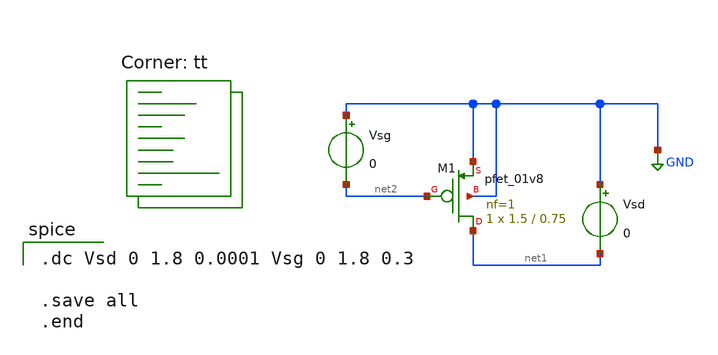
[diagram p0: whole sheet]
** sch_path: pmos_test.sch
**.subckt pmos_test
XM1 net1 net2 GND GND sky130_fd_pr__pfet_01v8 L=0.75 W=1.5 nf=1 ad='int((nf+1)/2) * W/nf * 0.29' as='int((nf+2)/2) * W/nf * 0.29'
+ pd='2*int((nf+1)/2) * (W/nf + 0.29)' ps='2*int((nf+2)/2) * (W/nf + 0.29)' nrd='0.29 / W' nrs='0.29 / W'
+ sa=0 sb=0 sd=0 mult=1 m=1
Vsd GND net1 0
Vsg GND net2 0
**** begin user architecture code
.lib $::SKYWATER_MODELS/sky130.lib.spice tt

.dc Vsd 0 1.8 0.0001 Vsg 0 1.8 0.3

.save all
.end

**** end user architecture code
**.ends
.GLOBAL GND
.end
